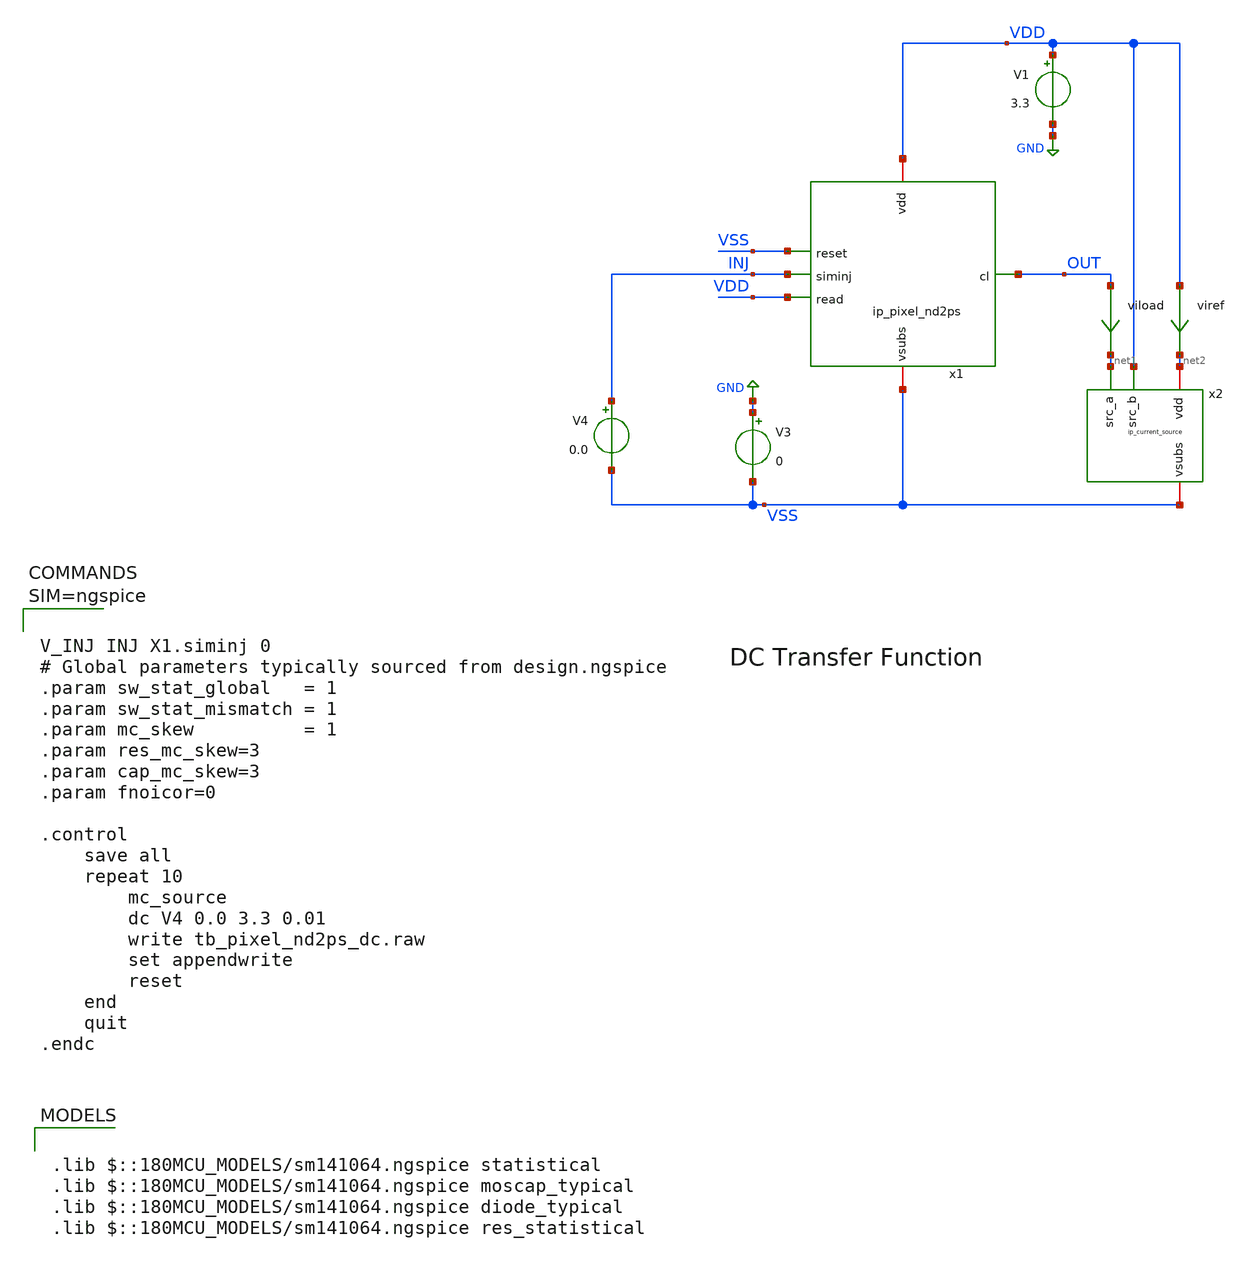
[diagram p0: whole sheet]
** sch_path: xschem/tb_pixel_nd2ps_dc.sch
**.subckt tb_pixel_nd2ps_dc
V1 VDD GND 3.3
V3 GND VSS 0
x1 VDD VSS INJ VDD VSS OUT ip_pixel_nd2ps
V4 INJ VSS 0.0
x2 net2 net1 VSS VDD ip_current_source
viload OUT net1 0
viref VDD net2 0
**** begin user architecture code

.lib $::180MCU_MODELS/sm141064.ngspice statistical
.lib $::180MCU_MODELS/sm141064.ngspice moscap_typical
.lib $::180MCU_MODELS/sm141064.ngspice diode_typical
.lib $::180MCU_MODELS/sm141064.ngspice res_statistical




V_INJ INJ X1.siminj 0
# Global parameters typically sourced from design.ngspice
.param sw_stat_global   = 1
.param sw_stat_mismatch = 1
.param mc_skew          = 1
.param res_mc_skew=3
.param cap_mc_skew=3
.param fnoicor=0

.control
	save all
	repeat 10
		mc_source
		dc V4 0.0 3.3 0.01
		write tb_pixel_nd2ps_dc.raw
		set appendwrite
		reset
	end
	quit
.endc



**** end user architecture code
**.ends

* expanding   symbol:  ip_pixel_nd2ps.sym # of pins=6
** sym_path: xschem/ip_pixel_nd2ps.sym
** sch_path: xschem/ip_pixel_nd2ps.sch
.subckt ip_pixel_nd2ps vdd reset siminj read vsubs cl
*.iopin vdd
*.iopin vsubs
*.ipin siminj
*.ipin reset
*.ipin read
*.opin cl
XM1 vdd reset siminj vsubs nfet_03v3 L=0.3u W=0.3u nf=1 ad='int((nf+1)/2) * W/nf * 0.18u' as='int((nf+2)/2) * W/nf * 0.18u'
+ pd='2*int((nf+1)/2) * (W/nf + 0.18u)' ps='2*int((nf+2)/2) * (W/nf + 0.18u)' nrd='0.18u / W' nrs='0.18u / W'
+ sa=0 sb=0 sd=0 m=1
XM2 vdd siminj sfout vsubs nfet_03v3 L=1u W=2.5u nf=1 ad='int((nf+1)/2) * W/nf * 0.18u' as='int((nf+2)/2) * W/nf * 0.18u'
+ pd='2*int((nf+1)/2) * (W/nf + 0.18u)' ps='2*int((nf+2)/2) * (W/nf + 0.18u)' nrd='0.18u / W' nrs='0.18u / W'
+ sa=0 sb=0 sd=0 m=1
XM3 sfout read cl vsubs nfet_03v3 L=0.3u W=0.3u nf=1 ad='int((nf+1)/2) * W/nf * 0.18u' as='int((nf+2)/2) * W/nf * 0.18u'
+ pd='2*int((nf+1)/2) * (W/nf + 0.18u)' ps='2*int((nf+2)/2) * (W/nf + 0.18u)' nrd='0.18u / W' nrs='0.18u / W'
+ sa=0 sb=0 sd=0 m=1
D1 vsubs siminj diode_nd2ps_03v3 area='13.5u * 13.5u ' pj='2*13.5u + 2*13.5u ' m=1
.ends


* expanding   symbol:  ip_current_source.sym # of pins=4
** sym_path: xschem/ip_current_source.sym
** sch_path: xschem/ip_current_source.sch
.subckt ip_current_source vdd src_a vsubs src_b
*.iopin vdd
*.iopin vsubs
*.ipin src_a
*.ipin src_b
XM8 refin refin vsubs vsubs nfet_06v0 L=1u W=5u nf=1 ad='int((nf+1)/2) * W/nf * 0.18u' as='int((nf+2)/2) * W/nf * 0.18u'
+ pd='2*int((nf+1)/2) * (W/nf + 0.18u)' ps='2*int((nf+2)/2) * (W/nf + 0.18u)' nrd='0.18u / W' nrs='0.18u / W'
+ sa=0 sb=0 sd=0 m=1 par=1
XM5 src_a refin net1 vsubs nfet_06v0 L=0.7u W=5u nf=1 ad='int((nf+1)/2) * W/nf * 0.18u' as='int((nf+2)/2) * W/nf * 0.18u'
+ pd='2*int((nf+1)/2) * (W/nf + 0.18u)' ps='2*int((nf+2)/2) * (W/nf + 0.18u)' nrd='0.18u / W' nrs='0.18u / W'
+ sa=0 sb=0 sd=0 m=2 par=2
XM3 src_b refin net2 vsubs nfet_06v0 L=0.7u W=5u nf=1 ad='int((nf+1)/2) * W/nf * 0.18u' as='int((nf+2)/2) * W/nf * 0.18u'
+ pd='2*int((nf+1)/2) * (W/nf + 0.18u)' ps='2*int((nf+2)/2) * (W/nf + 0.18u)' nrd='0.18u / W' nrs='0.18u / W'
+ sa=0 sb=0 sd=0 m=2 par=2
XM4 net1 refin vsubs vsubs nfet_06v0 L=5u W=0.5u nf=1 ad='int((nf+1)/2) * W/nf * 0.18u' as='int((nf+2)/2) * W/nf * 0.18u'
+ pd='2*int((nf+1)/2) * (W/nf + 0.18u)' ps='2*int((nf+2)/2) * (W/nf + 0.18u)' nrd='0.18u / W' nrs='0.18u / W'
+ sa=0 sb=0 sd=0 m=1 par=1
XM7 net2 refin vsubs vsubs nfet_06v0 L=5u W=0.5u nf=1 ad='int((nf+1)/2) * W/nf * 0.18u' as='int((nf+2)/2) * W/nf * 0.18u'
+ pd='2*int((nf+1)/2) * (W/nf + 0.18u)' ps='2*int((nf+2)/2) * (W/nf + 0.18u)' nrd='0.18u / W' nrs='0.18u / W'
+ sa=0 sb=0 sd=0 m=1 par=1
XR5 refin vdd vsubs ppolyf_u_1k_6p0 r_width=1e-6 r_length=42e-6 m=1
.ends

.GLOBAL GND
.end
